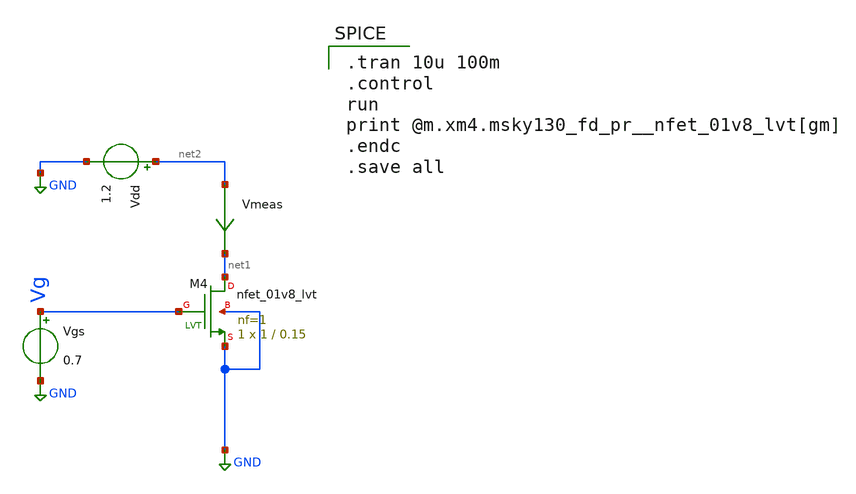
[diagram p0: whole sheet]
** sch_path: Blocks/Startup Converter/Vth_nmos_lvt.sch
**.subckt Vth_nmos_lvt
XM4 net1 Vg GND GND sky130_fd_pr__nfet_01v8_lvt L=0.15 W=1 nf=1 ad='int((nf+1)/2) * W/nf * 0.29' as='int((nf+2)/2) * W/nf * 0.29'
+ pd='2*int((nf+1)/2) * (W/nf + 0.29)' ps='2*int((nf+2)/2) * (W/nf + 0.29)' nrd='0.29 / W' nrs='0.29 / W'
+ sa=0 sb=0 sd=0 mult=1 m=1
Vgs Vg GND 0.7
Vmeas net2 net1 0
.save i(vmeas)
Vdd net2 GND 1.2
**** begin user architecture code

** opencircuitdesign pdks install
.lib $::SKYWATER_MODELS/sky130.lib.spice tt



.tran 10u 100m
.control
run
print @m.xm4.msky130_fd_pr__nfet_01v8_lvt[gm]
.endc
.save all

**** end user architecture code
**.ends
.GLOBAL GND
.end
